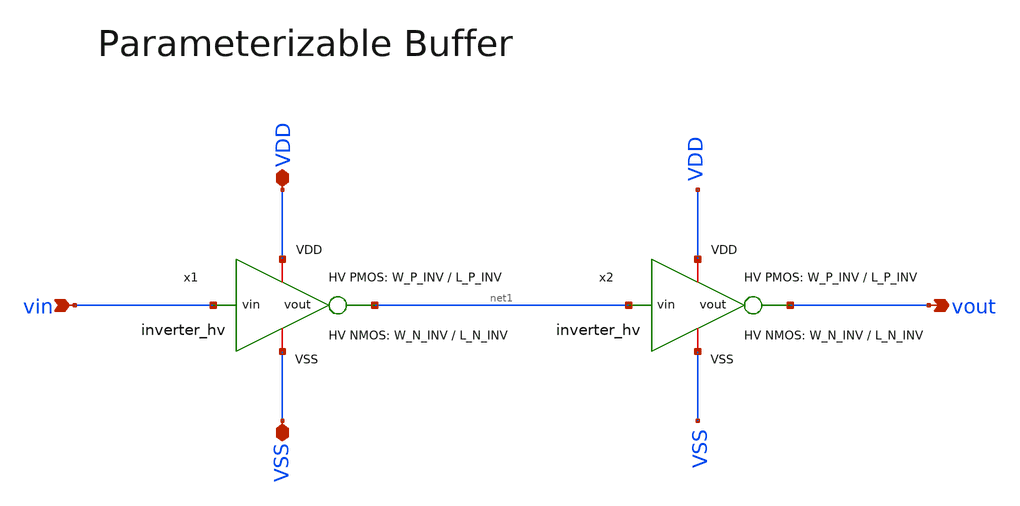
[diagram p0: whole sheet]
** sch_path: SG13G2_ATBS-ADC-main/xschem/buffer/buffer_hv.sch
**.subckt buffer_hv vin VDD VSS vout
*.ipin vin
*.iopin VDD
*.iopin VSS
*.opin vout
x1 VDD vin net1 VSS inverter_hv W_P=W_P_INV L_P=L_P_INV W_N=W_N_INV L_N=L_N_INV
x2 VDD net1 vout VSS inverter_hv W_P=W_P_INV L_P=L_P_INV W_N=W_N_INV L_N=L_N_INV
**.ends

* expanding   symbol:  inverter/inverter_hv.sym # of pins=4
** sym_path: SG13G2_ATBS-ADC-main/xschem/inverter/inverter_hv.sym
** sch_path: SG13G2_ATBS-ADC-main/xschem/inverter/inverter_hv.sch
.subckt inverter_hv VDD vin vout VSS  W_P=3.0u L_P=0.50u W_N=1.0u L_N=0.50u
*.ipin vin
*.iopin VDD
*.iopin VSS
*.opin vout
XM1 vout vin VDD VDD sg13_hv_pmos w=W_P l=L_P ng=1 m=1 mm_ok=1
XM2 vout vin VSS VSS sg13_hv_nmos w=W_N l=L_N ng=1 m=1 mm_ok=1
.ends

.end
